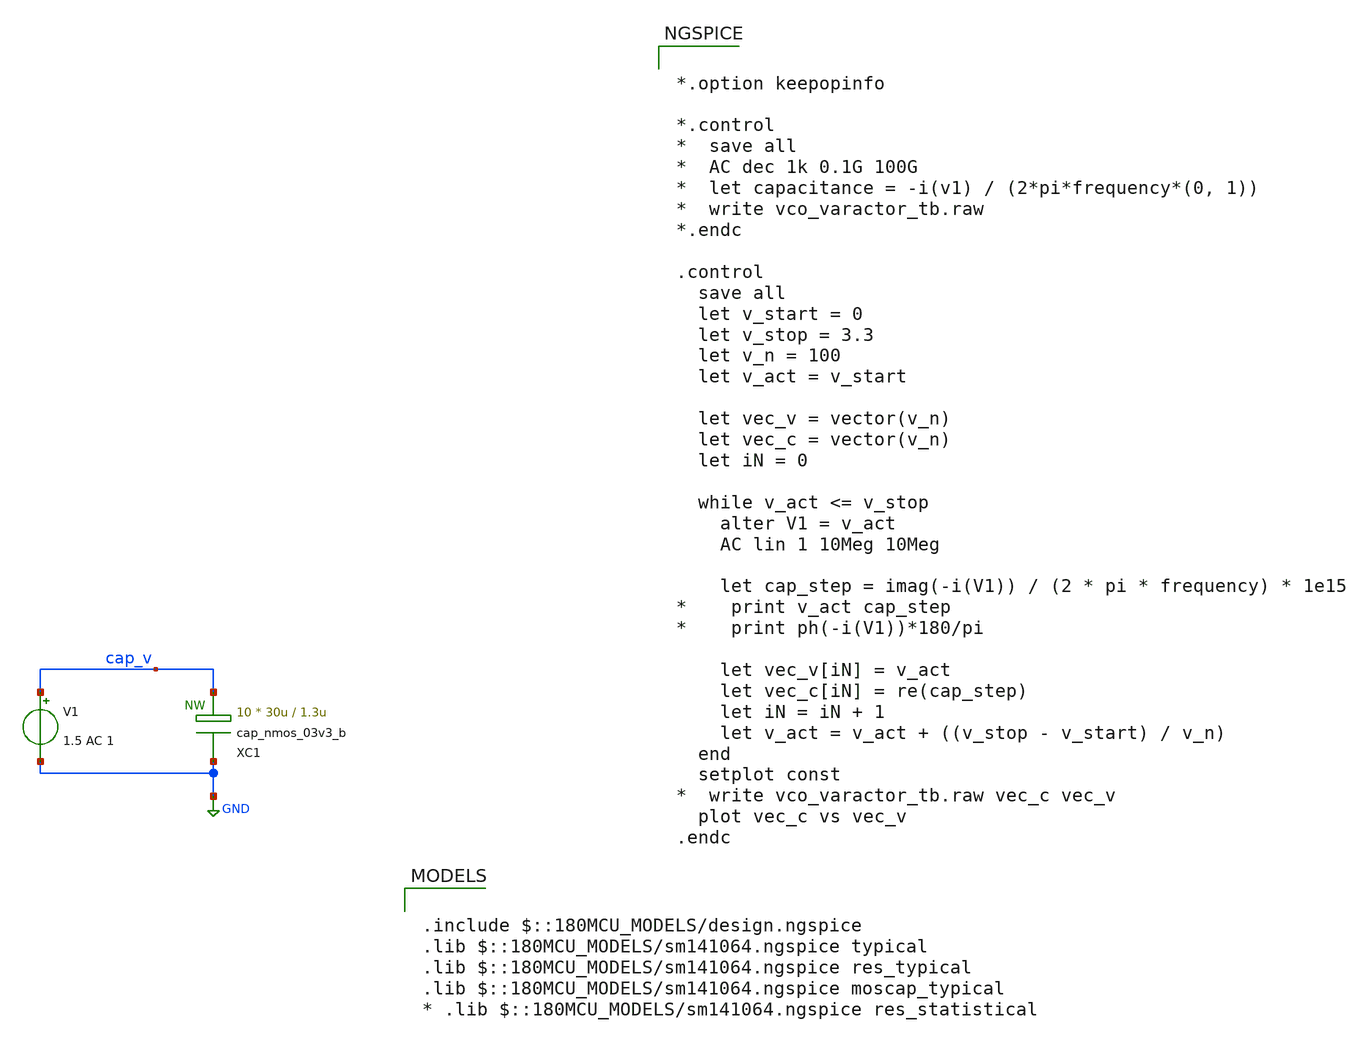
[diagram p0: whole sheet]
** sch_path: team_src/xschem/vco_varactor_tb.sch
**.subckt vco_varactor_tb
XC1 GND cap_v cap_nmos_03v3_b c_width=30u c_length=1.3u m=10
V1 cap_v GND 1.5 AC 1
.save i(v1)
**** begin user architecture code

.include $::180MCU_MODELS/design.ngspice
.lib $::180MCU_MODELS/sm141064.ngspice typical
.lib $::180MCU_MODELS/sm141064.ngspice res_typical
.lib $::180MCU_MODELS/sm141064.ngspice moscap_typical
* .lib $::180MCU_MODELS/sm141064.ngspice res_statistical



*.option keepopinfo

*.control
*  save all
*  AC dec 1k 0.1G 100G
*  let capacitance = -i(v1) / (2*pi*frequency*(0, 1))
*  write vco_varactor_tb.raw
*.endc

.control
  save all
  let v_start = 0
  let v_stop = 3.3
  let v_n = 100
  let v_act = v_start

  let vec_v = vector(v_n)
  let vec_c = vector(v_n)
  let iN = 0

  while v_act <= v_stop
    alter V1 = v_act
    AC lin 1 10Meg 10Meg

    let cap_step = imag(-i(V1)) / (2 * pi * frequency) * 1e15
*    print v_act cap_step
*    print ph(-i(V1))*180/pi

    let vec_v[iN] = v_act
    let vec_c[iN] = re(cap_step)
    let iN = iN + 1
    let v_act = v_act + ((v_stop - v_start) / v_n)
  end
  setplot const
*  write vco_varactor_tb.raw vec_c vec_v
  plot vec_c vs vec_v
.endc


**** end user architecture code
**.ends
.GLOBAL GND
.end
